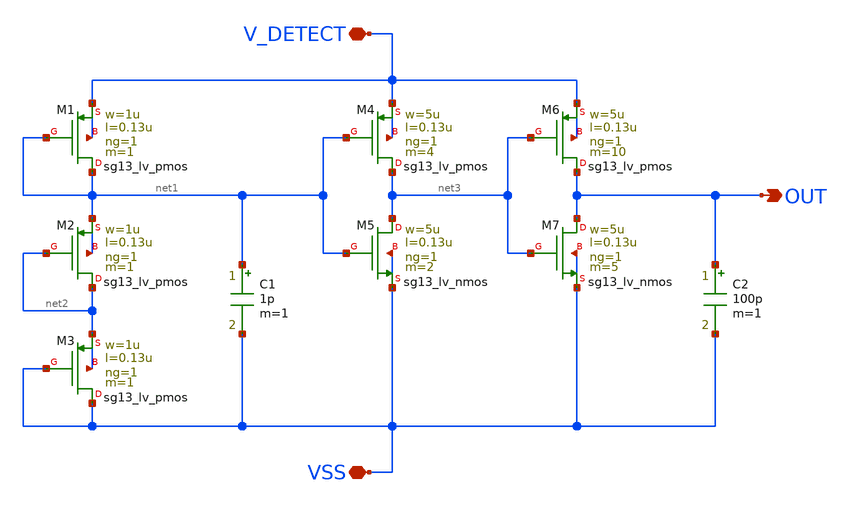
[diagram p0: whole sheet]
** sch_path: SSDOR_1V_v1/components/startup_ckt/startup_ckt.sch
**.subckt startup_ckt V_DETECT VSS OUT
*.iopin V_DETECT
*.iopin VSS
*.opin OUT
XM1 net1 net1 V_DETECT V_DETECT sg13_lv_pmos w=1u l=0.13u ng=1 m=1 mm_ok=1
XM2 net2 net2 net1 net1 sg13_lv_pmos w=1u l=0.13u ng=1 m=1 mm_ok=1
XM3 VSS VSS net2 net2 sg13_lv_pmos w=1u l=0.13u ng=1 m=1 mm_ok=1
XM4 net3 net1 V_DETECT V_DETECT sg13_lv_pmos w=5u l=0.13u ng=1 m=4 mm_ok=1
XM5 net3 net1 VSS VSS sg13_lv_nmos w=5u l=0.13u ng=1 m=2 mm_ok=1
C1 net1 VSS 1p m=1
XM6 OUT net3 V_DETECT V_DETECT sg13_lv_pmos w=5u l=0.13u ng=1 m=10 mm_ok=1
XM7 OUT net3 VSS VSS sg13_lv_nmos w=5u l=0.13u ng=1 m=5 mm_ok=1
C2 OUT VSS 100p m=1
**.ends
.end
